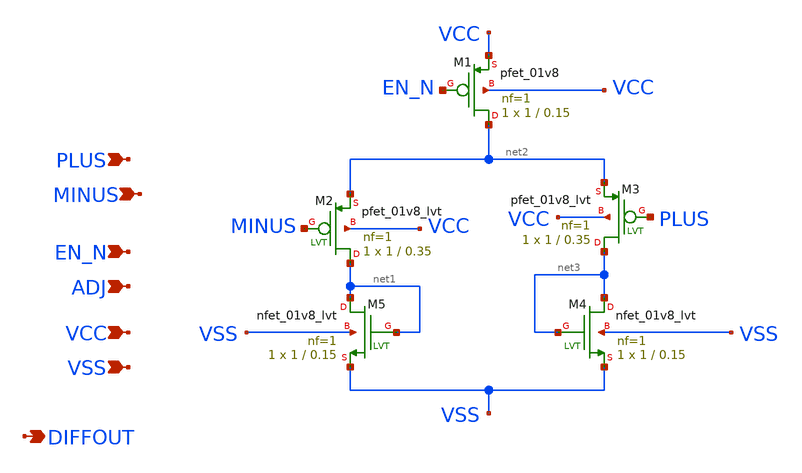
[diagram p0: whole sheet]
** sch_path: tuto.sch
**.subckt tuto PLUS MINUS VCC VSS EN_N ADJ DIFFOUT
*.ipin PLUS
*.ipin MINUS
*.ipin VCC
*.ipin VSS
*.ipin EN_N
*.ipin ADJ
*.opin DIFFOUT
XM1 net2 EN_N VCC VCC sky130_fd_pr__pfet_01v8 L=0.15 W=1 nf=1 ad='int((1 + 1)/2) * 1 / 1 * 0.29' as='int((1 + 2)/2) * 1 / 1 * 0.29'
+ pd='2*int((1 + 1)/2) * (1 / 1 + 0.29)' ps='2*int((1 + 2)/2) * (1 / 1 + 0.29)' nrd='0.29 / 1 ' nrs='0.29 / 1 '
+ sa=0 sb=0 sd=0 mult=1 m=1
XM2 net1 MINUS net2 VCC sky130_fd_pr__pfet_01v8_lvt L=0.35 W=1 nf=1 ad='int((1 + 1)/2) * 1 / 1 * 0.29'
+ as='int((1 + 2)/2) * 1 / 1 * 0.29' pd='2*int((1 + 1)/2) * (1 / 1 + 0.29)' ps='2*int((1 + 2)/2) * (1 / 1 + 0.29)'
+ nrd='0.29 / 1 ' nrs='0.29 / 1 ' sa=0 sb=0 sd=0 mult=1 m=1
XM3 net3 PLUS net2 VCC sky130_fd_pr__pfet_01v8_lvt L=0.35 W=1 nf=1 ad='int((1 + 1)/2) * 1 / 1 * 0.29'
+ as='int((1 + 2)/2) * 1 / 1 * 0.29' pd='2*int((1 + 1)/2) * (1 / 1 + 0.29)' ps='2*int((1 + 2)/2) * (1 / 1 + 0.29)'
+ nrd='0.29 / 1 ' nrs='0.29 / 1 ' sa=0 sb=0 sd=0 mult=1 m=1
XM5 net1 net1 VSS VSS sky130_fd_pr__nfet_01v8_lvt L=0.15 W=1 nf=1 ad='int((1 + 1)/2) * 1 / 1 * 0.29'
+ as='int((1 + 2)/2) * 1 / 1 * 0.29' pd='2*int((1 + 1)/2) * (1 / 1 + 0.29)' ps='2*int((1 + 2)/2) * (1 / 1 + 0.29)'
+ nrd='0.29 / 1 ' nrs='0.29 / 1 ' sa=0 sb=0 sd=0 mult=1 m=1
XM4 net3 net3 VSS VSS sky130_fd_pr__nfet_01v8_lvt L=0.15 W=1 nf=1 ad='int((1 + 1)/2) * 1 / 1 * 0.29'
+ as='int((1 + 2)/2) * 1 / 1 * 0.29' pd='2*int((1 + 1)/2) * (1 / 1 + 0.29)' ps='2*int((1 + 2)/2) * (1 / 1 + 0.29)'
+ nrd='0.29 / 1 ' nrs='0.29 / 1 ' sa=0 sb=0 sd=0 mult=1 m=1
**.ends
.end
